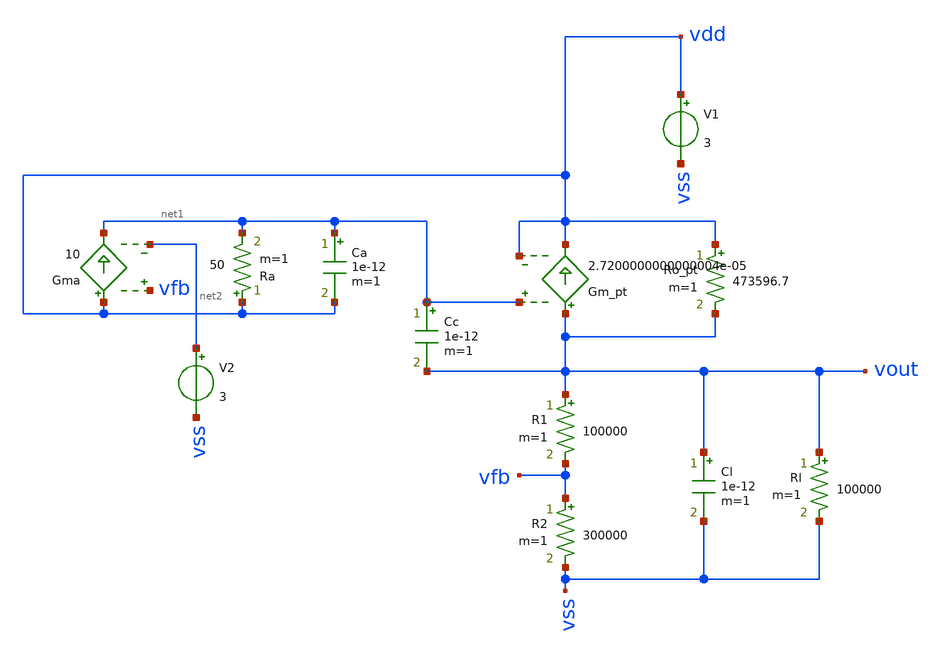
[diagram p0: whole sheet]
** sch_path: test-python/sstadex/xschem/ldo.sch
**.subckt ldo
Ro_pt vdd vout 473596.7 m=1
Gm_pt vout vdd net1 vdd 2.7200000000000004e-05
R1 vout vfb 100000 m=1
R2 vfb vss 300000 m=1
Gma vdd net1 vfb net2 10
Ra vdd net1 50 m=1
V1 vdd vss 3
V2 net2 vss 3
Cl vout vss 1e-12 m=1
Rl vout vss 100000 m=1
Ca net1 vdd 1e-12 m=1
Cc net1 vout 1e-12 m=1
**.ends
.end
